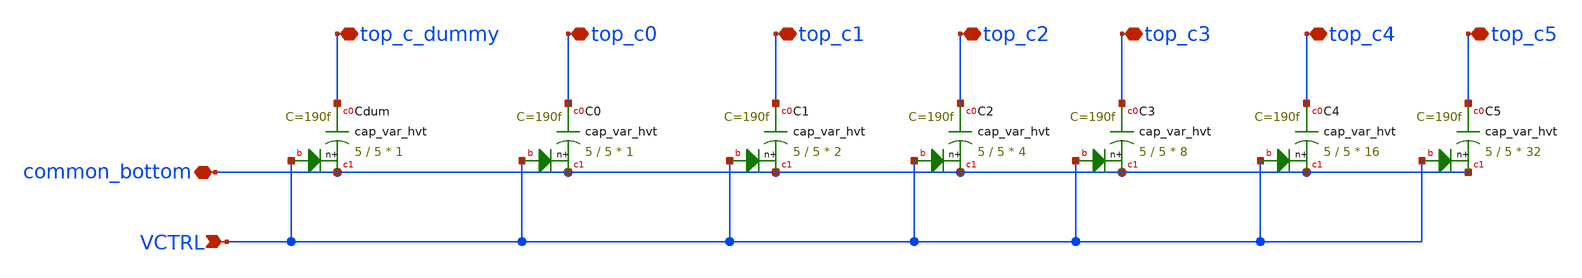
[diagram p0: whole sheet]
** sch_path: SKY130/SAR-ADC/SAR-ADC_5.0V/cap_array_var_MF.sch
**.subckt cap_array_var_MF common_bottom top_c1 top_c0 top_c_dummy top_c2 top_c4 top_c5 top_c3 VCTRL
*.iopin common_bottom
*.iopin top_c1
*.iopin top_c0
*.iopin top_c_dummy
*.iopin top_c2
*.iopin top_c4
*.iopin top_c5
*.iopin top_c3
*.ipin VCTRL
XC0 top_c0 common_bottom VCTRL sky130_fd_pr__cap_var_hvt W=5 L=5 VM=1 m=1
XC1 top_c1 common_bottom VCTRL sky130_fd_pr__cap_var_hvt W=5 L=5 VM=2 m=2
XC2 top_c2 common_bottom VCTRL sky130_fd_pr__cap_var_hvt W=5 L=5 VM=4 m=4
XC3 top_c3 common_bottom VCTRL sky130_fd_pr__cap_var_hvt W=5 L=5 VM=8 m=8
XC4 top_c4 common_bottom VCTRL sky130_fd_pr__cap_var_hvt W=5 L=5 VM=16 m=16
XC5 top_c5 common_bottom VCTRL sky130_fd_pr__cap_var_hvt W=5 L=5 VM=32 m=32
XCdum top_c_dummy common_bottom VCTRL sky130_fd_pr__cap_var_hvt W=5 L=5 VM=1 m=1
**.ends
.end
